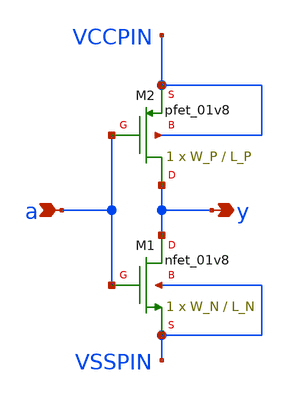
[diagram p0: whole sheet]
** sch_path: sky130_tests/not.sch
**.subckt not y a
*.opin y
*.ipin a
XM1 y a VSSPIN VSSPIN sky130_fd_pr__nfet_01v8 W=W_N L=L_N ad='W * 0.29' pd='W + 2 * 0.29' as='W * 0.29'
+ ps='W + 2 * 0.29' nrd=0 nrs=0 sa=0 sb=0 sd=0 nf=1 mult=1
XM2 y a VCCPIN VCCPIN sky130_fd_pr__pfet_01v8 W=W_P L=L_P ad='W * 0.29' pd='W + 2 * 0.29' as='W * 0.29'
+ ps='W + 2 * 0.29' nrd=0 nrs=0 sa=0 sb=0 sd=0 nf=1 mult=1
**.ends
.end
